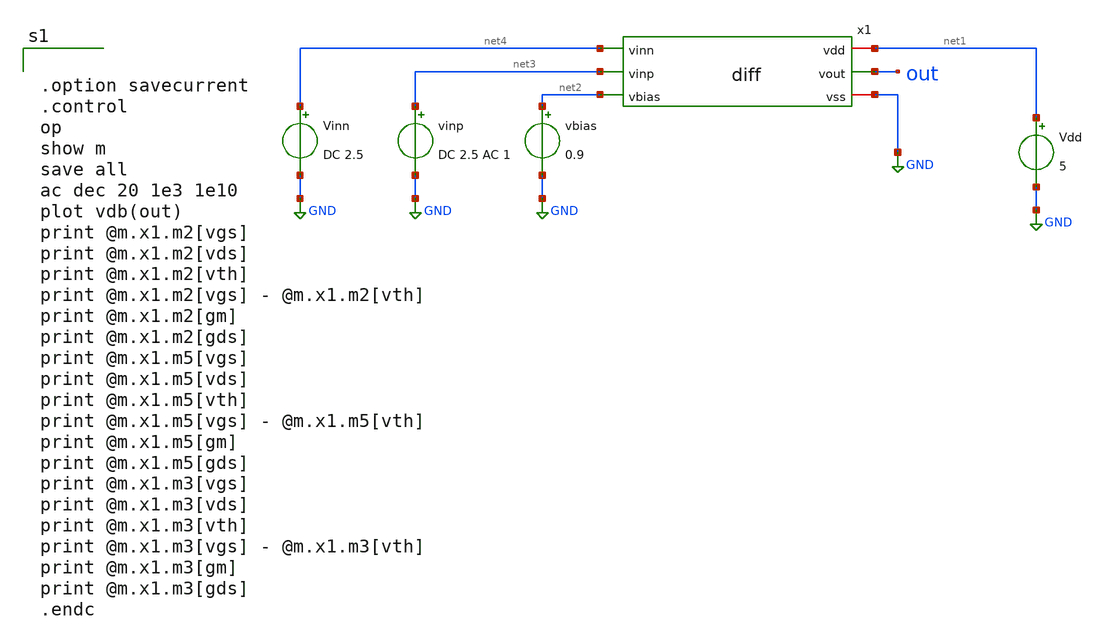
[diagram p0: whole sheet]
** sch_path: diff_ac.sch
**.subckt diff_ac
x1 net1 out net4 net3 net2 GND diff
Vinn net4 GND DC 2.5
vinp net3 GND DC 2.5 AC 1
vbias net2 GND 0.9
Vdd net1 GND 5
**** begin user architecture code
 .include $::LIB/mos.lib
.include $::LIB/passive.lib
.include $::LIB/diode.lib


.option savecurrent
.control
op
show m
save all
ac dec 20 1e3 1e10
plot vdb(out)
print @m.x1.m2[vgs]
print @m.x1.m2[vds]
print @m.x1.m2[vth]
print @m.x1.m2[vgs] - @m.x1.m2[vth]
print @m.x1.m2[gm]
print @m.x1.m2[gds]
print @m.x1.m5[vgs]
print @m.x1.m5[vds]
print @m.x1.m5[vth]
print @m.x1.m5[vgs] - @m.x1.m5[vth]
print @m.x1.m5[gm]
print @m.x1.m5[gds]
print @m.x1.m3[vgs]
print @m.x1.m3[vds]
print @m.x1.m3[vth]
print @m.x1.m3[vgs] - @m.x1.m3[vth]
print @m.x1.m3[gm]
print @m.x1.m3[gds]
.endc


**** end user architecture code
**.ends

* expanding   symbol:  diff.sym # of pins=6
** sym_path: diff.sym
** sch_path: diff.sch
.subckt diff vdd vout vinn vinp vbias vss
*.iopin vss
*.iopin vdd
*.ipin vinn
*.ipin vinp
*.opin vout
*.ipin vbias
M1 net1 vinn net2 vss nmos L=1u W=10u m=1
M2 vout vinp net2 vss nmos L=1u W=10u m=1
M3 net2 vbias vss vss nmos L=1u W=20u m=1
M4 net1 net1 vdd vdd pmos L=1u W=30u m=1
M5 vout net1 vdd vdd pmos L=1u W=30u m=1
.ends

.GLOBAL GND
.end
